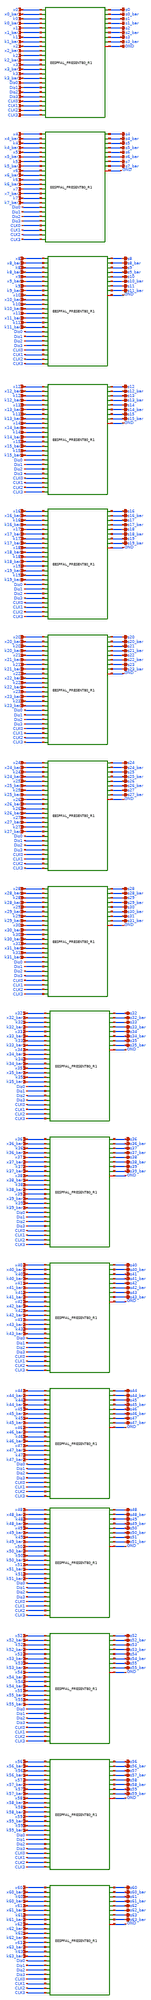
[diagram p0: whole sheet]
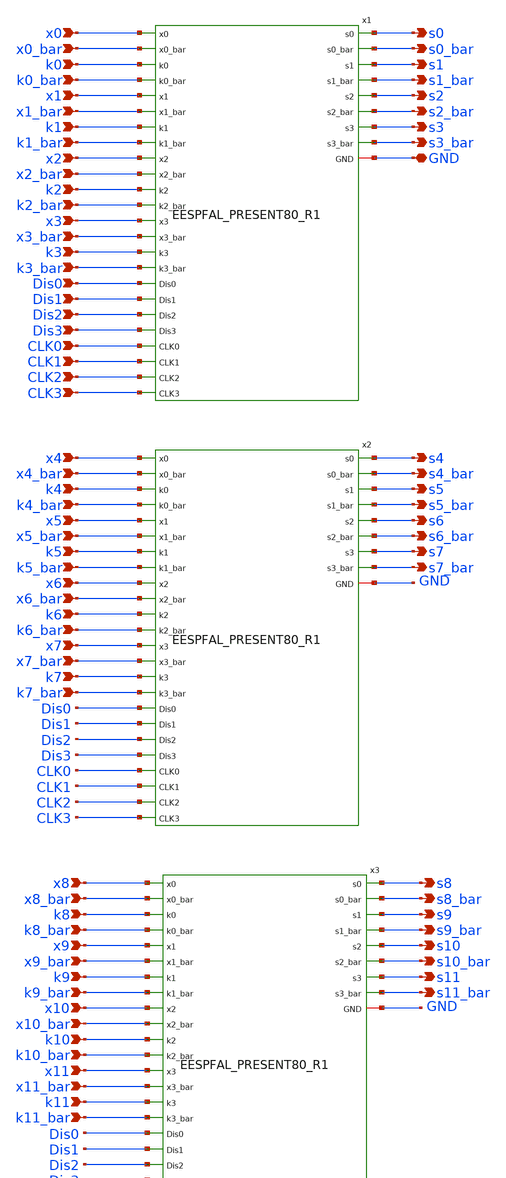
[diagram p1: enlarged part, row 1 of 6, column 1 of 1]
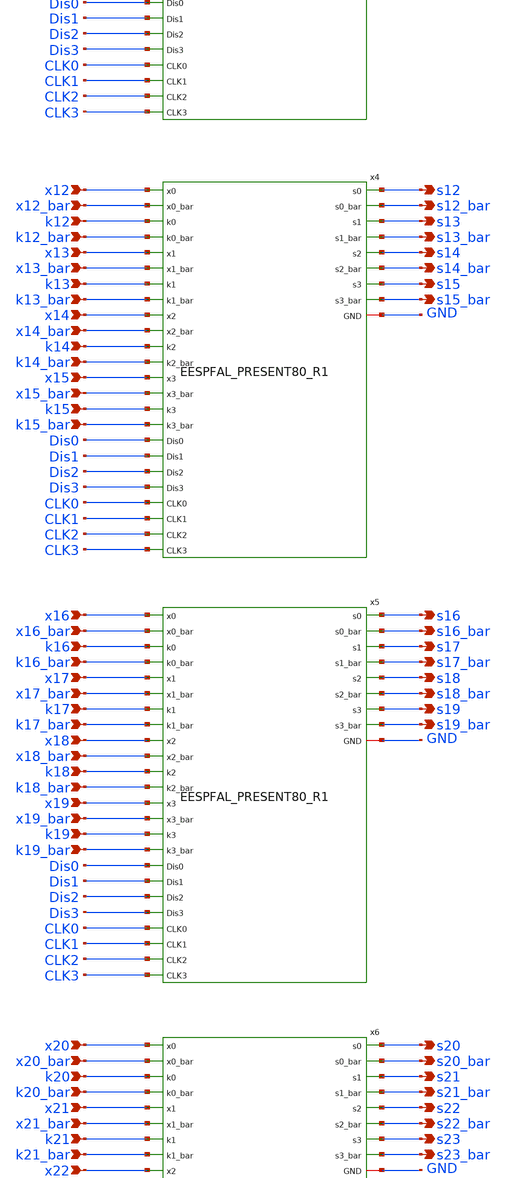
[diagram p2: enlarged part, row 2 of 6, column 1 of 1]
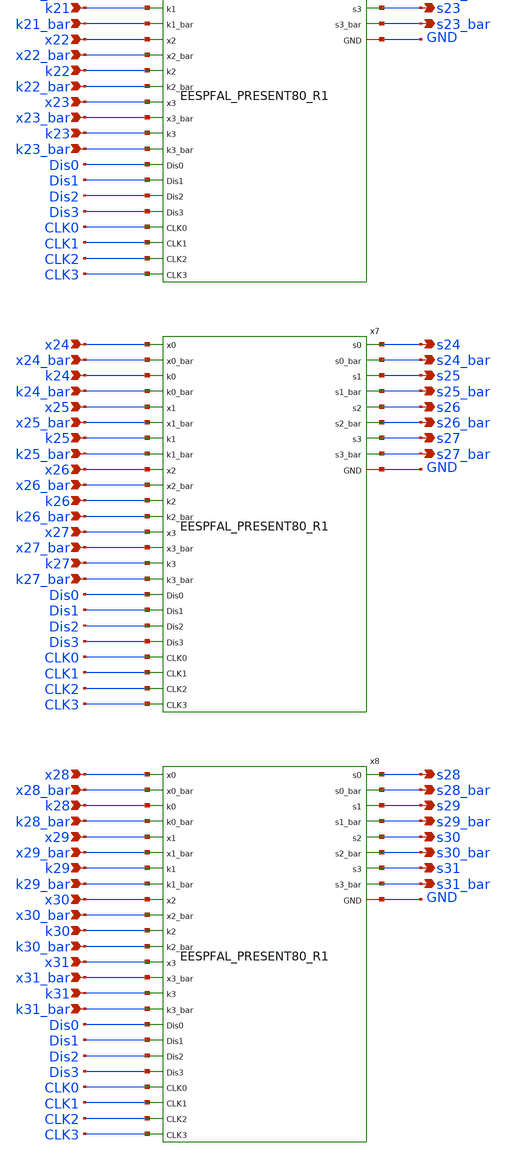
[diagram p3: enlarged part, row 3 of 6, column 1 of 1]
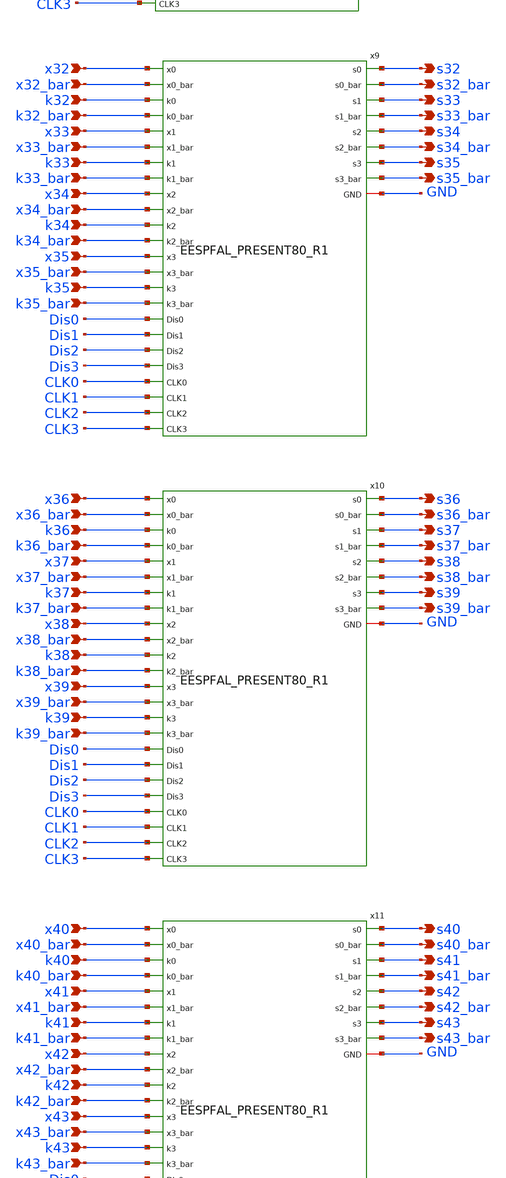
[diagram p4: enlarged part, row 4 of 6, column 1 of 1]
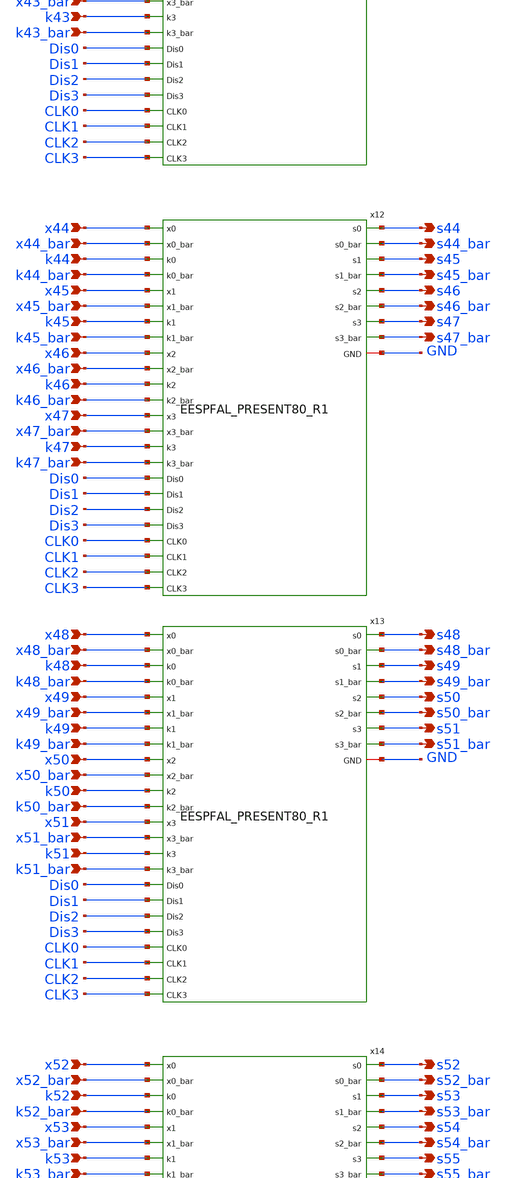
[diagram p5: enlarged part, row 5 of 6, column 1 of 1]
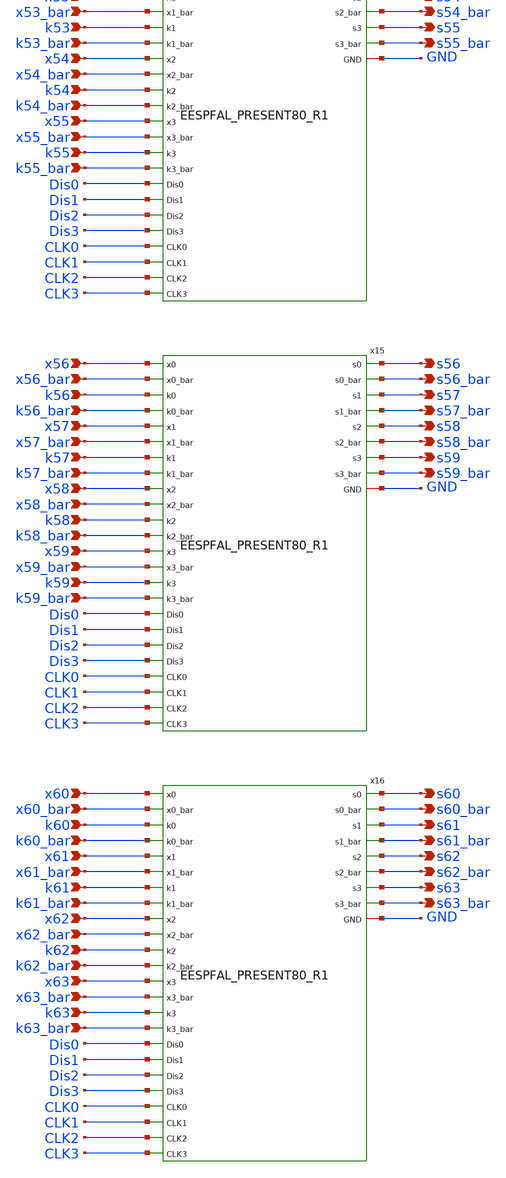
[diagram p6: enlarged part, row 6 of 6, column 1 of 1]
** sch_path: skywater_stuff/EESPFAL_64bitwidth_PRESENT80_R1.sch
**.subckt EESPFAL_64bitwidth_PRESENT80_R1 x4 x4_bar k4 k4_bar x5 x5_bar k5 k5_bar x6 x6_bar k6
*+ k6_bar x7 x7_bar k7 k7_bar x8 x8_bar k8 k8_bar x9 x9_bar k9 k9_bar x10 x10_bar k10 k10_bar x11 x11_bar k11
*+ k11_bar x12 x12_bar k12 k12_bar x13 x13_bar k13 k13_bar x14 x14_bar k14 k14_bar x15 x15_bar k15 k15_bar x16
*+ x16_bar k16 k16_bar x17 x17_bar k17 k17_bar x18 x18_bar k18 k18_bar x19 x19_bar k19 k19_bar x20 x20_bar k20
*+ k20_bar x21 x21_bar k21 k21_bar x22 x22_bar k22 k22_bar x23 x23_bar k23 k23_bar x24 x24_bar k24 k24_bar x25
*+ x25_bar k25 k25_bar x26 x26_bar k26 k26_bar x27 x27_bar k27 k27_bar x28 x28_bar k28 k28_bar x29 x29_bar k29
*+ k29_bar x30 x30_bar k30 k30_bar x31 x31_bar k31 k31_bar x32 x32_bar k32 k32_bar x33 x33_bar k33 k33_bar x34
*+ x34_bar k34 k34_bar x35 x35_bar k35 k35_bar x36 x36_bar k36 k36_bar x37 x37_bar k37 k37_bar x38 x38_bar k38
*+ k38_bar x39 x39_bar k39 k39_bar x40 x40_bar k40 k40_bar x41 x41_bar k41 k41_bar x42 x42_bar k42 k42_bar x43
*+ x43_bar k43 k43_bar x44 x44_bar k44 k44_bar x45 x45_bar k45 k45_bar x46 x46_bar k46 k46_bar x47 x47_bar k47
*+ k47_bar x48 x48_bar k48 k48_bar x49 x49_bar k49 k49_bar x50 x50_bar k50 k50_bar x51 x51_bar k51 k51_bar x52
*+ x52_bar k52 k52_bar x53 x53_bar k53 k53_bar x54 x54_bar k54 k54_bar x55 x55_bar k55 k55_bar x56 x56_bar k56
*+ k56_bar x57 x57_bar k57 k57_bar x58 x58_bar k58 k58_bar x59 x59_bar k59 k59_bar x60 x60_bar k60 k60_bar x61
*+ x61_bar k61 k61_bar x62 x62_bar k62 k62_bar x63 x63_bar k63 k63_bar x0 x0_bar k0 k0_bar x1 x1_bar k1 k1_bar
*+ x2 x2_bar k2 k2_bar x3 x3_bar k3 k3_bar Dis0 Dis1 CLK0 Dis2 Dis3 CLK1 CLK2 CLK3 s0 s0_bar s1 s1_bar s2
*+ s2_bar s3 s3_bar s4 s4_bar s5 s5_bar s6 s6_bar s7 s7_bar s8 s8_bar s9 s9_bar s10 s10_bar s11 s11_bar s12
*+ s12_bar s13 s13_bar s14 s14_bar s15 s15_bar s16 s16_bar s17 s17_bar s18 s18_bar s19 s19_bar s20 s20_bar s21
*+ s21_bar s22 s22_bar s23 s23_bar s24 s24_bar s25 s25_bar s26 s26_bar s27 s27_bar s28 s28_bar s29 s29_bar s30
*+ s30_bar s31 s31_bar s32 s32_bar s33 s33_bar s34 s34_bar s35 s35_bar s36 s36_bar s37 s37_bar s38 s38_bar s39
*+ s39_bar s40 s40_bar s41 s41_bar s42 s42_bar s43 s43_bar s44 s44_bar s45 s45_bar s46 s46_bar s47 s47_bar s48
*+ s48_bar s49 s49_bar s50 s50_bar s51 s51_bar s52 s52_bar s53 s53_bar s54 s54_bar s55 s55_bar s56 s56_bar s57
*+ s57_bar s58 s58_bar s59 s59_bar s60 s60_bar s61 s61_bar s62 s62_bar s63 s63_bar GND
*.ipin x4
*.ipin x4_bar
*.ipin k4
*.ipin k4_bar
*.ipin x5
*.ipin x5_bar
*.ipin k5
*.ipin k5_bar
*.ipin x6
*.ipin x6_bar
*.ipin k6
*.ipin k6_bar
*.ipin x7
*.ipin x7_bar
*.ipin k7
*.ipin k7_bar
*.ipin x8
*.ipin x8_bar
*.ipin k8
*.ipin k8_bar
*.ipin x9
*.ipin x9_bar
*.ipin k9
*.ipin k9_bar
*.ipin x10
*.ipin x10_bar
*.ipin k10
*.ipin k10_bar
*.ipin x11
*.ipin x11_bar
*.ipin k11
*.ipin k11_bar
*.ipin x12
*.ipin x12_bar
*.ipin k12
*.ipin k12_bar
*.ipin x13
*.ipin x13_bar
*.ipin k13
*.ipin k13_bar
*.ipin x14
*.ipin x14_bar
*.ipin k14
*.ipin k14_bar
*.ipin x15
*.ipin x15_bar
*.ipin k15
*.ipin k15_bar
*.ipin x16
*.ipin x16_bar
*.ipin k16
*.ipin k16_bar
*.ipin x17
*.ipin x17_bar
*.ipin k17
*.ipin k17_bar
*.ipin x18
*.ipin x18_bar
*.ipin k18
*.ipin k18_bar
*.ipin x19
*.ipin x19_bar
*.ipin k19
*.ipin k19_bar
*.ipin x20
*.ipin x20_bar
*.ipin k20
*.ipin k20_bar
*.ipin x21
*.ipin x21_bar
*.ipin k21
*.ipin k21_bar
*.ipin x22
*.ipin x22_bar
*.ipin k22
*.ipin k22_bar
*.ipin x23
*.ipin x23_bar
*.ipin k23
*.ipin k23_bar
*.ipin x24
*.ipin x24_bar
*.ipin k24
*.ipin k24_bar
*.ipin x25
*.ipin x25_bar
*.ipin k25
*.ipin k25_bar
*.ipin x26
*.ipin x26_bar
*.ipin k26
*.ipin k26_bar
*.ipin x27
*.ipin x27_bar
*.ipin k27
*.ipin k27_bar
*.ipin x28
*.ipin x28_bar
*.ipin k28
*.ipin k28_bar
*.ipin x29
*.ipin x29_bar
*.ipin k29
*.ipin k29_bar
*.ipin x30
*.ipin x30_bar
*.ipin k30
*.ipin k30_bar
*.ipin x31
*.ipin x31_bar
*.ipin k31
*.ipin k31_bar
*.ipin x32
*.ipin x32_bar
*.ipin k32
*.ipin k32_bar
*.ipin x33
*.ipin x33_bar
*.ipin k33
*.ipin k33_bar
*.ipin x34
*.ipin x34_bar
*.ipin k34
*.ipin k34_bar
*.ipin x35
*.ipin x35_bar
*.ipin k35
*.ipin k35_bar
*.ipin x36
*.ipin x36_bar
*.ipin k36
*.ipin k36_bar
*.ipin x37
*.ipin x37_bar
*.ipin k37
*.ipin k37_bar
*.ipin x38
*.ipin x38_bar
*.ipin k38
*.ipin k38_bar
*.ipin x39
*.ipin x39_bar
*.ipin k39
*.ipin k39_bar
*.ipin x40
*.ipin x40_bar
*.ipin k40
*.ipin k40_bar
*.ipin x41
*.ipin x41_bar
*.ipin k41
*.ipin k41_bar
*.ipin x42
*.ipin x42_bar
*.ipin k42
*.ipin k42_bar
*.ipin x43
*.ipin x43_bar
*.ipin k43
*.ipin k43_bar
*.ipin x44
*.ipin x44_bar
*.ipin k44
*.ipin k44_bar
*.ipin x45
*.ipin x45_bar
*.ipin k45
*.ipin k45_bar
*.ipin x46
*.ipin x46_bar
*.ipin k46
*.ipin k46_bar
*.ipin x47
*.ipin x47_bar
*.ipin k47
*.ipin k47_bar
*.ipin x48
*.ipin x48_bar
*.ipin k48
*.ipin k48_bar
*.ipin x49
*.ipin x49_bar
*.ipin k49
*.ipin k49_bar
*.ipin x50
*.ipin x50_bar
*.ipin k50
*.ipin k50_bar
*.ipin x51
*.ipin x51_bar
*.ipin k51
*.ipin k51_bar
*.ipin x52
*.ipin x52_bar
*.ipin k52
*.ipin k52_bar
*.ipin x53
*.ipin x53_bar
*.ipin k53
*.ipin k53_bar
*.ipin x54
*.ipin x54_bar
*.ipin k54
*.ipin k54_bar
*.ipin x55
*.ipin x55_bar
*.ipin k55
*.ipin k55_bar
*.ipin x56
*.ipin x56_bar
*.ipin k56
*.ipin k56_bar
*.ipin x57
*.ipin x57_bar
*.ipin k57
*.ipin k57_bar
*.ipin x58
*.ipin x58_bar
*.ipin k58
*.ipin k58_bar
*.ipin x59
*.ipin x59_bar
*.ipin k59
*.ipin k59_bar
*.ipin x60
*.ipin x60_bar
*.ipin k60
*.ipin k60_bar
*.ipin x61
*.ipin x61_bar
*.ipin k61
*.ipin k61_bar
*.ipin x62
*.ipin x62_bar
*.ipin k62
*.ipin k62_bar
*.ipin x63
*.ipin x63_bar
*.ipin k63
*.ipin k63_bar
*.ipin x0
*.ipin x0_bar
*.ipin k0
*.ipin k0_bar
*.ipin x1
*.ipin x1_bar
*.ipin k1
*.ipin k1_bar
*.ipin x2
*.ipin x2_bar
*.ipin k2
*.ipin k2_bar
*.ipin x3
*.ipin x3_bar
*.ipin k3
*.ipin k3_bar
*.ipin Dis0
*.ipin Dis1
*.ipin CLK0
*.ipin Dis2
*.ipin Dis3
*.ipin CLK1
*.ipin CLK2
*.ipin CLK3
*.opin s0
*.opin s0_bar
*.opin s1
*.opin s1_bar
*.opin s2
*.opin s2_bar
*.opin s3
*.opin s3_bar
*.opin s4
*.opin s4_bar
*.opin s5
*.opin s5_bar
*.opin s6
*.opin s6_bar
*.opin s7
*.opin s7_bar
*.opin s8
*.opin s8_bar
*.opin s9
*.opin s9_bar
*.opin s10
*.opin s10_bar
*.opin s11
*.opin s11_bar
*.opin s12
*.opin s12_bar
*.opin s13
*.opin s13_bar
*.opin s14
*.opin s14_bar
*.opin s15
*.opin s15_bar
*.opin s16
*.opin s16_bar
*.opin s17
*.opin s17_bar
*.opin s18
*.opin s18_bar
*.opin s19
*.opin s19_bar
*.opin s20
*.opin s20_bar
*.opin s21
*.opin s21_bar
*.opin s22
*.opin s22_bar
*.opin s23
*.opin s23_bar
*.opin s24
*.opin s24_bar
*.opin s25
*.opin s25_bar
*.opin s26
*.opin s26_bar
*.opin s27
*.opin s27_bar
*.opin s28
*.opin s28_bar
*.opin s29
*.opin s29_bar
*.opin s30
*.opin s30_bar
*.opin s31
*.opin s31_bar
*.opin s32
*.opin s32_bar
*.opin s33
*.opin s33_bar
*.opin s34
*.opin s34_bar
*.opin s35
*.opin s35_bar
*.opin s36
*.opin s36_bar
*.opin s37
*.opin s37_bar
*.opin s38
*.opin s38_bar
*.opin s39
*.opin s39_bar
*.opin s40
*.opin s40_bar
*.opin s41
*.opin s41_bar
*.opin s42
*.opin s42_bar
*.opin s43
*.opin s43_bar
*.opin s44
*.opin s44_bar
*.opin s45
*.opin s45_bar
*.opin s46
*.opin s46_bar
*.opin s47
*.opin s47_bar
*.opin s48
*.opin s48_bar
*.opin s49
*.opin s49_bar
*.opin s50
*.opin s50_bar
*.opin s51
*.opin s51_bar
*.opin s52
*.opin s52_bar
*.opin s53
*.opin s53_bar
*.opin s54
*.opin s54_bar
*.opin s55
*.opin s55_bar
*.opin s56
*.opin s56_bar
*.opin s57
*.opin s57_bar
*.opin s58
*.opin s58_bar
*.opin s59
*.opin s59_bar
*.opin s60
*.opin s60_bar
*.opin s61
*.opin s61_bar
*.opin s62
*.opin s62_bar
*.opin s63
*.opin s63_bar
*.iopin GND
x1 GND x0 x0_bar k0 k0_bar x1 x1_bar k1 k1_bar x2 x2_bar k2 k2_bar x3 x3_bar k3 k3_bar s0 s0_bar
+ CLK0 Dis0 CLK1 Dis1 s2 s2_bar s3_bar s3 s1_bar s1 CLK3 Dis2 CLK2 Dis3 EESPFAL_PRESENT80_R1
x2 GND x4 x4_bar k4 k4_bar x5 x5_bar k5 k5_bar x6 x6_bar k6 k6_bar x7 x7_bar k7 k7_bar s4 s4_bar
+ CLK0 Dis0 CLK1 Dis1 s6 s6_bar s7_bar s7 s5_bar s5 CLK3 Dis2 CLK2 Dis3 EESPFAL_PRESENT80_R1
x3 GND x8 x8_bar k8 k8_bar x9 x9_bar k9 k9_bar x10 x10_bar k10 k10_bar x11 x11_bar k11 k11_bar s8
+ s8_bar CLK0 Dis0 CLK1 Dis1 s10 s10_bar s11_bar s11 s9_bar s9 CLK3 Dis2 CLK2 Dis3 EESPFAL_PRESENT80_R1
x4 GND x12 x12_bar k12 k12_bar x13 x13_bar k13 k13_bar x14 x14_bar k14 k14_bar x15 x15_bar k15
+ k15_bar s12 s12_bar CLK0 Dis0 CLK1 Dis1 s14 s14_bar s15_bar s15 s13_bar s13 CLK3 Dis2 CLK2 Dis3
+ EESPFAL_PRESENT80_R1
x5 GND x16 x16_bar k16 k16_bar x17 x17_bar k17 k17_bar x18 x18_bar k18 k18_bar x19 x19_bar k19
+ k19_bar s16 s16_bar CLK0 Dis0 CLK1 Dis1 s18 s18_bar s19_bar s19 s17_bar s17 CLK3 Dis2 CLK2 Dis3
+ EESPFAL_PRESENT80_R1
x6 GND x20 x20_bar k20 k20_bar x21 x21_bar k21 k21_bar x22 x22_bar k22 k22_bar x23 x23_bar k23
+ k23_bar s20 s20_bar CLK0 Dis0 CLK1 Dis1 s22 s22_bar s23_bar s23 s21_bar s21 CLK3 Dis2 CLK2 Dis3
+ EESPFAL_PRESENT80_R1
x7 GND x24 x24_bar k24 k24_bar x25 x25_bar k25 k25_bar x26 x26_bar k26 k26_bar x27 x27_bar k27
+ k27_bar s24 s24_bar CLK0 Dis0 CLK1 Dis1 s26 s26_bar s27_bar s27 s25_bar s25 CLK3 Dis2 CLK2 Dis3
+ EESPFAL_PRESENT80_R1
x8 GND x28 x28_bar k28 k28_bar x29 x29_bar k29 k29_bar x30 x30_bar k30 k30_bar x31 x31_bar k31
+ k31_bar s28 s28_bar CLK0 Dis0 CLK1 Dis1 s30 s30_bar s31_bar s31 s29_bar s29 CLK3 Dis2 CLK2 Dis3
+ EESPFAL_PRESENT80_R1
x9 GND x32 x32_bar k32 k32_bar x33 x33_bar k33 k33_bar x34 x34_bar k34 k34_bar x35 x35_bar k35
+ k35_bar s32 s32_bar CLK0 Dis0 CLK1 Dis1 s34 s34_bar s35_bar s35 s33_bar s33 CLK3 Dis2 CLK2 Dis3
+ EESPFAL_PRESENT80_R1
x10 GND x36 x36_bar k36 k36_bar x37 x37_bar k37 k37_bar x38 x38_bar k38 k38_bar x39 x39_bar k39
+ k39_bar s36 s36_bar CLK0 Dis0 CLK1 Dis1 s38 s38_bar s39_bar s39 s37_bar s37 CLK3 Dis2 CLK2 Dis3
+ EESPFAL_PRESENT80_R1
x11 GND x40 x40_bar k40 k40_bar x41 x41_bar k41 k41_bar x42 x42_bar k42 k42_bar x43 x43_bar k43
+ k43_bar s40 s40_bar CLK0 Dis0 CLK1 Dis1 s42 s42_bar s43_bar s43 s41_bar s41 CLK3 Dis2 CLK2 Dis3
+ EESPFAL_PRESENT80_R1
x12 GND x44 x44_bar k44 k44_bar x45 x45_bar k45 k45_bar x46 x46_bar k46 k46_bar x47 x47_bar k47
+ k47_bar s44 s44_bar CLK0 Dis0 CLK1 Dis1 s46 s46_bar s47_bar s47 s45_bar s45 CLK3 Dis2 CLK2 Dis3
+ EESPFAL_PRESENT80_R1
x13 GND x48 x48_bar k48 k48_bar x49 x49_bar k49 k49_bar x50 x50_bar k50 k50_bar x51 x51_bar k51
+ k51_bar s48 s48_bar CLK0 Dis0 CLK1 Dis1 s50 s50_bar s51_bar s51 s49_bar s49 CLK3 Dis2 CLK2 Dis3
+ EESPFAL_PRESENT80_R1
x14 GND x52 x52_bar k52 k52_bar x53 x53_bar k53 k53_bar x54 x54_bar k54 k54_bar x55 x55_bar k55
+ k55_bar s52 s52_bar CLK0 Dis0 CLK1 Dis1 s54 s54_bar s55_bar s55 s53_bar s53 CLK3 Dis2 CLK2 Dis3
+ EESPFAL_PRESENT80_R1
x15 GND x56 x56_bar k56 k56_bar x57 x57_bar k57 k57_bar x58 x58_bar k58 k58_bar x59 x59_bar k59
+ k59_bar s56 s56_bar CLK0 Dis0 CLK1 Dis1 s58 s58_bar s59_bar s59 s57_bar s57 CLK3 Dis2 CLK2 Dis3
+ EESPFAL_PRESENT80_R1
x16 GND x60 x60_bar k60 k60_bar x61 x61_bar k61 k61_bar x62 x62_bar k62 k62_bar x63 x63_bar k63
+ k63_bar s60 s60_bar CLK0 Dis0 CLK1 Dis1 s62 s62_bar s63_bar s63 s61_bar s61 CLK3 Dis2 CLK2 Dis3
+ EESPFAL_PRESENT80_R1
**.ends
.end
